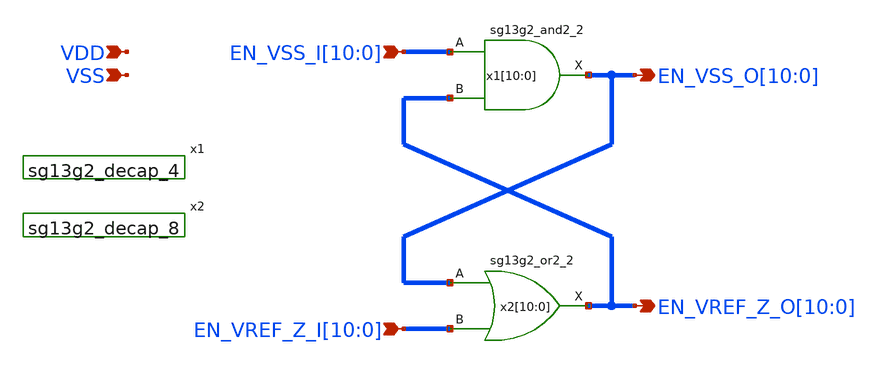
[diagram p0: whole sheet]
** sch_path: schematic/break_before_make/break_before_make.sch
* IHP-GmbH/IHP-Open-PDK/ihp-sg13g2/libs.tech/xschem/sg13g2_stdcells/sg13g2_decap_4.sch:
* Copyright 2023 IHP PDK Authors
* Licensed under the Apache License, Version 2.0 (the "License");
**.subckt break_before_make
*+ EN_VSS_I[10],EN_VSS_I[9],EN_VSS_I[8],EN_VSS_I[7],EN_VSS_I[6],EN_VSS_I[5],EN_VSS_I[4],EN_VSS_I[3],EN_VSS_I[2],EN_VSS_I[1],EN_VSS_I[0]
*+ EN_VREF_Z_I[10],EN_VREF_Z_I[9],EN_VREF_Z_I[8],EN_VREF_Z_I[7],EN_VREF_Z_I[6],EN_VREF_Z_I[5],EN_VREF_Z_I[4],EN_VREF_Z_I[3],EN_VREF_Z_I[2],EN_VREF_Z_I[1],EN_VREF_Z_I[0] VDD VSS
*+ EN_VSS_O[10],EN_VSS_O[9],EN_VSS_O[8],EN_VSS_O[7],EN_VSS_O[6],EN_VSS_O[5],EN_VSS_O[4],EN_VSS_O[3],EN_VSS_O[2],EN_VSS_O[1],EN_VSS_O[0]
*+ EN_VREF_Z_O[10],EN_VREF_Z_O[9],EN_VREF_Z_O[8],EN_VREF_Z_O[7],EN_VREF_Z_O[6],EN_VREF_Z_O[5],EN_VREF_Z_O[4],EN_VREF_Z_O[3],EN_VREF_Z_O[2],EN_VREF_Z_O[1],EN_VREF_Z_O[0]
*.ipin
*+ EN_VSS_I[10],EN_VSS_I[9],EN_VSS_I[8],EN_VSS_I[7],EN_VSS_I[6],EN_VSS_I[5],EN_VSS_I[4],EN_VSS_I[3],EN_VSS_I[2],EN_VSS_I[1],EN_VSS_I[0]
*.ipin
*+ EN_VREF_Z_I[10],EN_VREF_Z_I[9],EN_VREF_Z_I[8],EN_VREF_Z_I[7],EN_VREF_Z_I[6],EN_VREF_Z_I[5],EN_VREF_Z_I[4],EN_VREF_Z_I[3],EN_VREF_Z_I[2],EN_VREF_Z_I[1],EN_VREF_Z_I[0]
*.ipin VDD
*.ipin VSS
*.opin
*+ EN_VSS_O[10],EN_VSS_O[9],EN_VSS_O[8],EN_VSS_O[7],EN_VSS_O[6],EN_VSS_O[5],EN_VSS_O[4],EN_VSS_O[3],EN_VSS_O[2],EN_VSS_O[1],EN_VSS_O[0]
*.opin
*+ EN_VREF_Z_O[10],EN_VREF_Z_O[9],EN_VREF_Z_O[8],EN_VREF_Z_O[7],EN_VREF_Z_O[6],EN_VREF_Z_O[5],EN_VREF_Z_O[4],EN_VREF_Z_O[3],EN_VREF_Z_O[2],EN_VREF_Z_O[1],EN_VREF_Z_O[0]
x1[10] EN_VSS_O[10] EN_VSS_I[10] EN_VREF_Z_O[10] VDD VSS sg13g2_and2_2
x1[9] EN_VSS_O[9] EN_VSS_I[9] EN_VREF_Z_O[9] VDD VSS sg13g2_and2_2
x1[8] EN_VSS_O[8] EN_VSS_I[8] EN_VREF_Z_O[8] VDD VSS sg13g2_and2_2
x1[7] EN_VSS_O[7] EN_VSS_I[7] EN_VREF_Z_O[7] VDD VSS sg13g2_and2_2
x1[6] EN_VSS_O[6] EN_VSS_I[6] EN_VREF_Z_O[6] VDD VSS sg13g2_and2_2
x1[5] EN_VSS_O[5] EN_VSS_I[5] EN_VREF_Z_O[5] VDD VSS sg13g2_and2_2
x1[4] EN_VSS_O[4] EN_VSS_I[4] EN_VREF_Z_O[4] VDD VSS sg13g2_and2_2
x1[3] EN_VSS_O[3] EN_VSS_I[3] EN_VREF_Z_O[3] VDD VSS sg13g2_and2_2
x1[2] EN_VSS_O[2] EN_VSS_I[2] EN_VREF_Z_O[2] VDD VSS sg13g2_and2_2
x1[1] EN_VSS_O[1] EN_VSS_I[1] EN_VREF_Z_O[1] VDD VSS sg13g2_and2_2
x1[0] EN_VSS_O[0] EN_VSS_I[0] EN_VREF_Z_O[0] VDD VSS sg13g2_and2_2
x2[10] EN_VREF_Z_O[10] EN_VSS_O[10] EN_VREF_Z_I[10] VDD VSS sg13g2_or2_2
x2[9] EN_VREF_Z_O[9] EN_VSS_O[9] EN_VREF_Z_I[9] VDD VSS sg13g2_or2_2
x2[8] EN_VREF_Z_O[8] EN_VSS_O[8] EN_VREF_Z_I[8] VDD VSS sg13g2_or2_2
x2[7] EN_VREF_Z_O[7] EN_VSS_O[7] EN_VREF_Z_I[7] VDD VSS sg13g2_or2_2
x2[6] EN_VREF_Z_O[6] EN_VSS_O[6] EN_VREF_Z_I[6] VDD VSS sg13g2_or2_2
x2[5] EN_VREF_Z_O[5] EN_VSS_O[5] EN_VREF_Z_I[5] VDD VSS sg13g2_or2_2
x2[4] EN_VREF_Z_O[4] EN_VSS_O[4] EN_VREF_Z_I[4] VDD VSS sg13g2_or2_2
x2[3] EN_VREF_Z_O[3] EN_VSS_O[3] EN_VREF_Z_I[3] VDD VSS sg13g2_or2_2
x2[2] EN_VREF_Z_O[2] EN_VSS_O[2] EN_VREF_Z_I[2] VDD VSS sg13g2_or2_2
x2[1] EN_VREF_Z_O[1] EN_VSS_O[1] EN_VREF_Z_I[1] VDD VSS sg13g2_or2_2
x2[0] EN_VREF_Z_O[0] EN_VSS_O[0] EN_VREF_Z_I[0] VDD VSS sg13g2_or2_2
x1 VDD VSS sg13g2_decap_4
x2 VDD VSS sg13g2_decap_8
**.ends

* expanding   symbol:  sg13g2_stdcells/sg13g2_and2_2.sym # of pins=3
** sym_path: sg13g2_stdcells/sg13g2_and2_2.sym
** sch_path: sg13g2_stdcells/sg13g2_and2_2.sch
.subckt sg13g2_and2_2 X A B VDD VSS
*.ipin A
*.ipin B
*.opin X
*.iopin VDD
*.iopin VSS
XM1 net1 A net2 VSS sg13_lv_nmos w=640.00n l=130.00n ng=1 m=1 mm_ok=1
XM2 net2 B VSS VSS sg13_lv_nmos w=640.00n l=130.00n ng=1 m=1 mm_ok=1
XM3 X net1 VSS VSS sg13_lv_nmos w=1.48u l=130.00n ng=2 m=1 mm_ok=1
XM4 net1 B VDD VDD sg13_lv_pmos w=840.00n l=130.00n ng=1 m=1 mm_ok=1
XM5 net1 A VDD VDD sg13_lv_pmos w=840.00n l=130.00n ng=1 m=1 mm_ok=1
XM6 X net1 VDD VDD sg13_lv_pmos w=2.24u l=130.00n ng=2 m=1 mm_ok=1
.ends


* expanding   symbol:  sg13g2_stdcells/sg13g2_or2_2.sym # of pins=3
** sym_path: sg13g2_stdcells/sg13g2_or2_2.sym
** sch_path: sg13g2_stdcells/sg13g2_or2_2.sch
.subckt sg13g2_or2_2 X A B VDD VSS
*.opin X
*.ipin B
*.ipin A
*.iopin VDD
*.iopin VSS
XM1 net1 B VSS VSS sg13_lv_nmos w=550.00n l=130.00n ng=1 m=1 mm_ok=1
XM2 net1 A VSS VSS sg13_lv_nmos w=550.00n l=130.00n ng=1 m=1 mm_ok=1
XM3 X net1 VSS VSS sg13_lv_nmos w=1.48u l=130.00n ng=2 m=1 mm_ok=1
XM4 net2 A VDD VDD sg13_lv_pmos w=840.00n l=130.00n ng=1 m=1 mm_ok=1
XM5 net1 B net2 VDD sg13_lv_pmos w=840.00n l=130.00n ng=1 m=1 mm_ok=1
XM6 X net1 VDD VDD sg13_lv_pmos w=2.24u l=130.00n ng=2 m=1 mm_ok=1
.ends


* expanding   symbol:  sg13g2_stdcells/sg13g2_decap_4.sym # of pins=0
** sym_path: sg13g2_stdcells/sg13g2_decap_4.sym
** sch_path: sg13g2_stdcells/sg13g2_decap_4.sch
.subckt sg13g2_decap_4 VDD VSS
*.iopin VDD
*.iopin VSS
XM1 VSS VDD VSS VSS sg13_lv_nmos w=420.00n l=1.000u ng=1 m=1 mm_ok=1
XM2 VDD VSS VDD VDD sg13_lv_pmos w=1.000u l=1.000u ng=1 m=1 mm_ok=1
.ends


* expanding   symbol:  sg13g2_stdcells/sg13g2_decap_8.sym # of pins=0
** sym_path: sg13g2_stdcells/sg13g2_decap_8.sym
** sch_path: sg13g2_stdcells/sg13g2_decap_8.sch
.subckt sg13g2_decap_8 VDD VSS
*.iopin VDD
*.iopin VSS
XM1 VSS VDD VSS VSS sg13_lv_nmos w=840.00n l=1.000u ng=2 m=1 mm_ok=1
XM2 VDD VSS VDD VDD sg13_lv_pmos w=2.000u l=1.000u ng=2 m=1 mm_ok=1
.ends

.end
